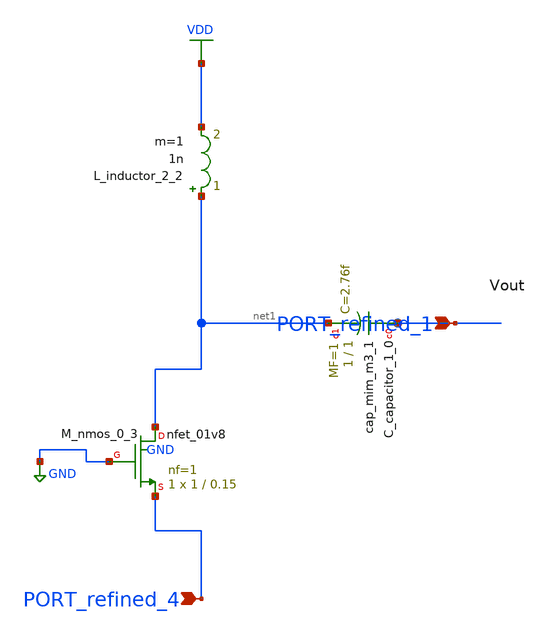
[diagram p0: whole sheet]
** sch_path: schematics/SchemGen/no_doi_41_001.sch
**.subckt no_doi_41_001 PORT_refined_4 PORT_refined_1
*.ipin PORT_refined_4
*.ipin PORT_refined_1
XC_capacitor_1_0 PORT_refined_1 net1 sky130_fd_pr__cap_mim_m3_1 W=1 L=1 MF=1 m=1
L_inductor_2_2 net1 VDD 1n m=1
XM_nmos_0_3 net1 GND PORT_refined_4 GND sky130_fd_pr__nfet_01v8 L=0.15 W=1 nf=1 ad='int((1 + 1)/2) * 1 / 1 * 0.29'
+ as='int((1 + 2)/2) * 1 / 1 * 0.29' pd='2*int((1 + 1)/2) * (1 / 1 + 0.29)' ps='2*int((1 + 2)/2) * (1 / 1 + 0.29)'
+ nrd='0.29 / 1 ' nrs='0.29 / 1 ' sa=0 sb=0 sd=0 mult=1 m=1
**.ends
.GLOBAL GND
.GLOBAL VDD
.end
